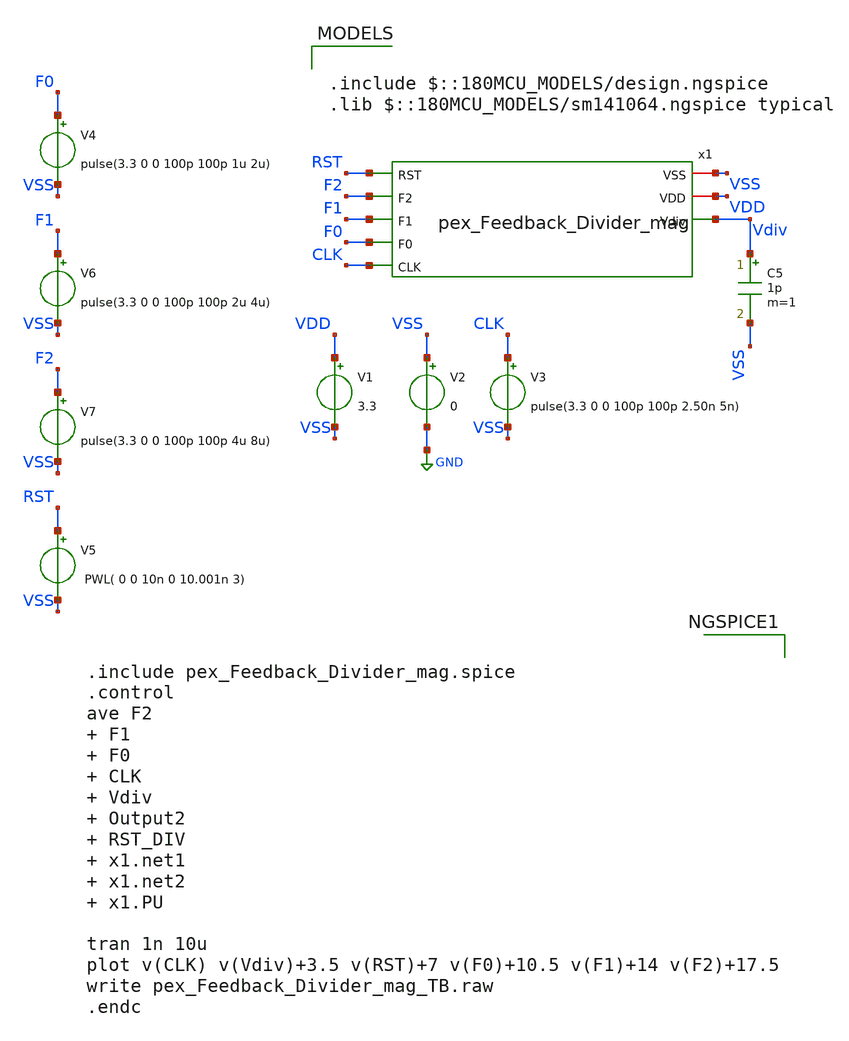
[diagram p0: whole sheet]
** sch_path: Clock_Generator_PAKISTAN_02/xschem/pex_Feedback_Divider_mag_TB.sch
**.subckt pex_Feedback_Divider_mag_TB
V1 VDD VSS 3.3
V2 VSS GND 0
V3 CLK VSS pulse(3.3 0 0 100p 100p 2.50n 5n)
C5 Vdiv VSS 1p m=1
V5 RST VSS PWL( 0 0 10n 0 10.001n 3)
V4 F0 VSS pulse(3.3 0 0 100p 100p 1u 2u)
V6 F1 VSS pulse(3.3 0 0 100p 100p 2u 4u)
V7 F2 VSS pulse(3.3 0 0 100p 100p 4u 8u)
x1 VSS VDD RST Vdiv F2 F1 F0 CLK pex_Feedback_Divider_mag
**** begin user architecture code

.include $::180MCU_MODELS/design.ngspice
.lib $::180MCU_MODELS/sm141064.ngspice typical



.include pex_Feedback_Divider_mag.spice
.control
ave F2  F1  F0  CLK  Vdiv  Output2  RST_DIV  x1.net1  x1.net2  x1.PU

tran 1n 10u
plot v(CLK) v(Vdiv)+3.5 v(RST)+7 v(F0)+10.5 v(F1)+14 v(F2)+17.5
write pex_Feedback_Divider_mag_TB.raw
.endc


**** end user architecture code
**.ends
.GLOBAL GND
.end
